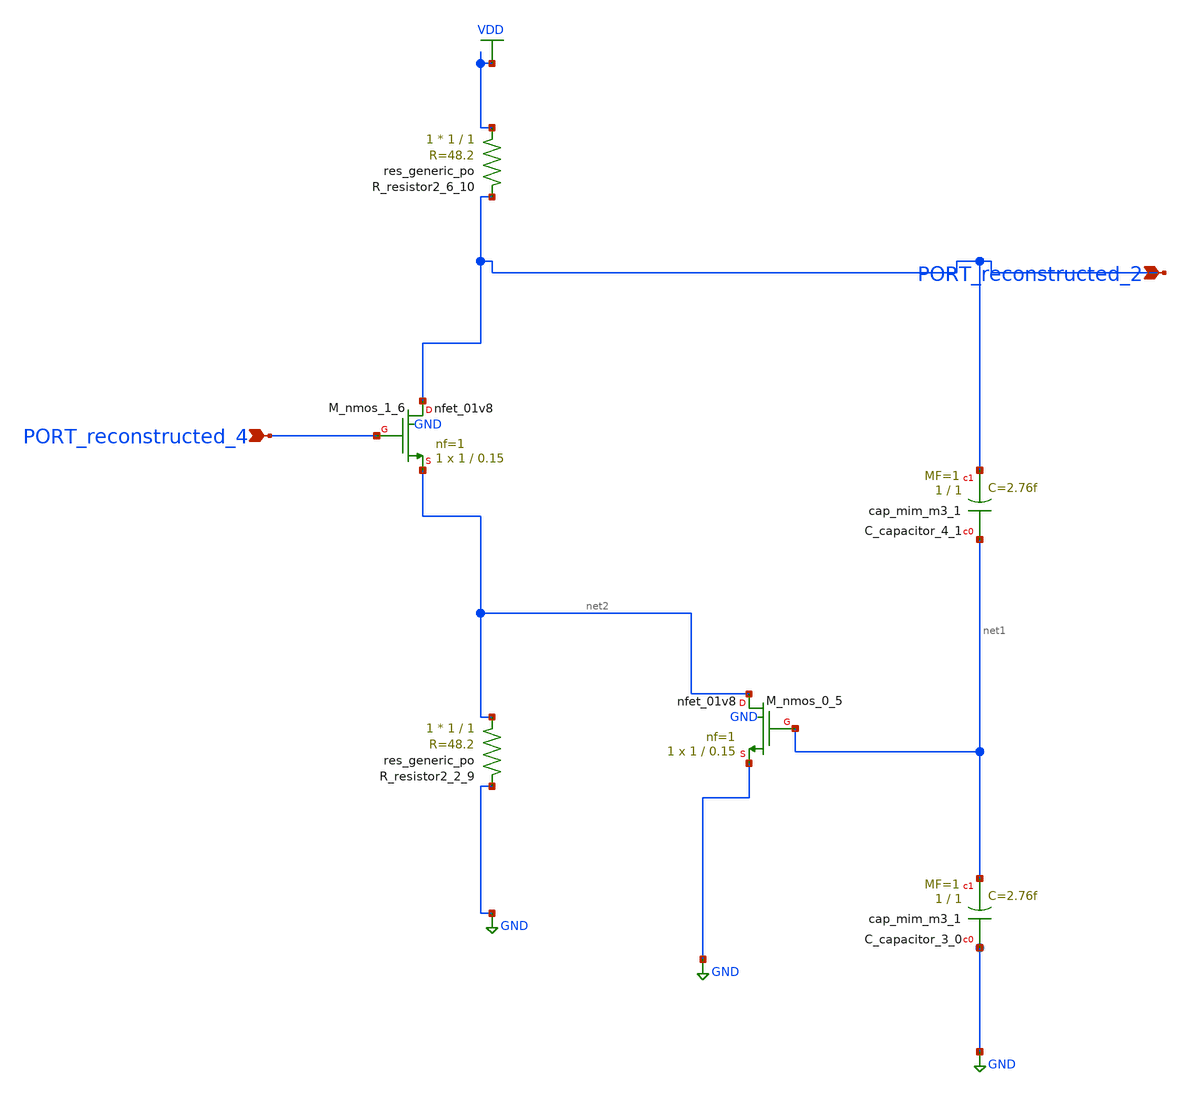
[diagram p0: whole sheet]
** sch_path: schematics/AMSNet/544.sch
**.subckt 544 PORT_reconstructed_2 PORT_reconstructed_4
*.ipin PORT_reconstructed_2
*.ipin PORT_reconstructed_4
XC_capacitor_3_0 GND net1 sky130_fd_pr__cap_mim_m3_1 W=1 L=1 MF=1 m=1
XC_capacitor_4_1 net1 PORT_reconstructed_2 sky130_fd_pr__cap_mim_m3_1 W=1 L=1 MF=1 m=1
XM_nmos_0_5 net2 net1 GND GND sky130_fd_pr__nfet_01v8 L=0.15 W=1 nf=1 ad='int((1 + 1)/2) * 1 / 1 * 0.29'
+ as='int((1 + 2)/2) * 1 / 1 * 0.29' pd='2*int((1 + 1)/2) * (1 / 1 + 0.29)' ps='2*int((1 + 2)/2) * (1 / 1 + 0.29)'
+ nrd='0.29 / 1 ' nrs='0.29 / 1 ' sa=0 sb=0 sd=0 mult=1 m=1
XM_nmos_1_6 PORT_reconstructed_2 PORT_reconstructed_4 net2 GND sky130_fd_pr__nfet_01v8 L=0.15 W=1 nf=1
+ ad='int((1 + 1)/2) * 1 / 1 * 0.29' as='int((1 + 2)/2) * 1 / 1 * 0.29' pd='2*int((1 + 1)/2) * (1 / 1 + 0.29)'
+ ps='2*int((1 + 2)/2) * (1 / 1 + 0.29)' nrd='0.29 / 1 ' nrs='0.29 / 1 ' sa=0 sb=0 sd=0 mult=1 m=1
XR_resistor2_2_9 net2 GND sky130_fd_pr__res_generic_po W=1 L=1 m=1
XR_resistor2_6_10 VDD PORT_reconstructed_2 sky130_fd_pr__res_generic_po W=1 L=1 m=1
**.ends
.GLOBAL GND
.GLOBAL VDD
.end
